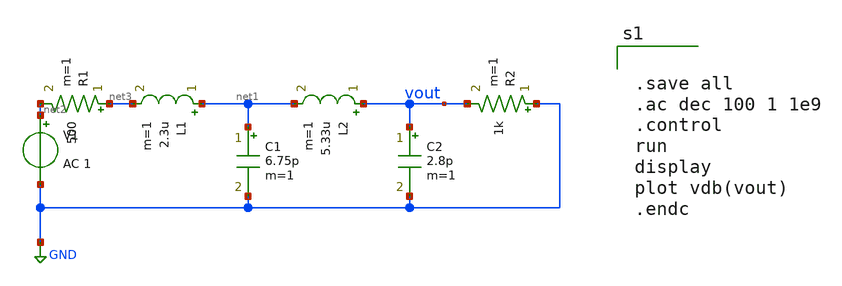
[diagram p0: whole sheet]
** sch_path: xschem/lclpf_test.sch
**.subckt lclpf_test
L1 net1 net3 2.3u m=1
L2 vout net1 5.33u m=1
C1 net1 GND 6.75p m=1
C2 vout GND 2.8p m=1
R2 GND vout 1k m=1
V1 net2 GND AC 1
R1 net3 net2 500 m=1
**** begin user architecture code


.save all
.ac dec 100 1 1e9
.control
run
display
plot vdb(vout)
.endc

**** end user architecture code
**.ends
.GLOBAL GND
.end
